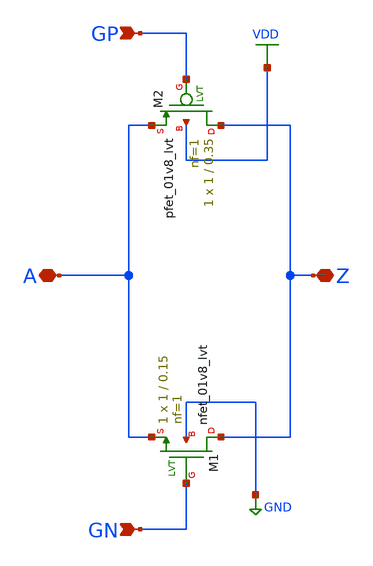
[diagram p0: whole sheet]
** sch_path: xschem/dacpassgate.sch
* Copyright 2021 Stefan Frederik Schippers
* Licensed under the Apache License, Version 2.0 (the "License");
* you may not use this file except in compliance with the License.
* You may obtain a copy of the License at
* https://www.apache.org/licenses/LICENSE-2.0
* Unless required by applicable law or agreed to in writing, software
* distributed under the License is distributed on an "AS IS" BASIS,
* WITHOUT WARRANTIES OR CONDITIONS OF ANY KIND, either express or implied.
* See the License for the specific language governing permissions and
* limitations under the License.
**.subckt dacpassgate A Z GP GN
*.iopin A
*.iopin Z
*.ipin GP
*.ipin GN
XM2 Z GP A VDD sky130_fd_pr__pfet_01v8_lvt L=0.35 W=1 nf=1 ad='int((nf+1)/2) * W/nf * 0.29' as='int((nf+2)/2) * W/nf * 0.29'
+ pd='2*int((nf+1)/2) * (W/nf + 0.29)' ps='2*int((nf+2)/2) * (W/nf + 0.29)' nrd='0.29 / W' nrs='0.29 / W'
+ sa=0 sb=0 sd=0 mult=1 m=1
XM1 Z GN A GND sky130_fd_pr__nfet_01v8_lvt L=0.15 W=1 nf=1 ad='int((nf+1)/2) * W/nf * 0.29' as='int((nf+2)/2) * W/nf * 0.29'
+ pd='2*int((nf+1)/2) * (W/nf + 0.29)' ps='2*int((nf+2)/2) * (W/nf + 0.29)' nrd='0.29 / W' nrs='0.29 / W'
+ sa=0 sb=0 sd=0 mult=1 m=1
**.ends
.GLOBAL GND
.GLOBAL VDD
.end
